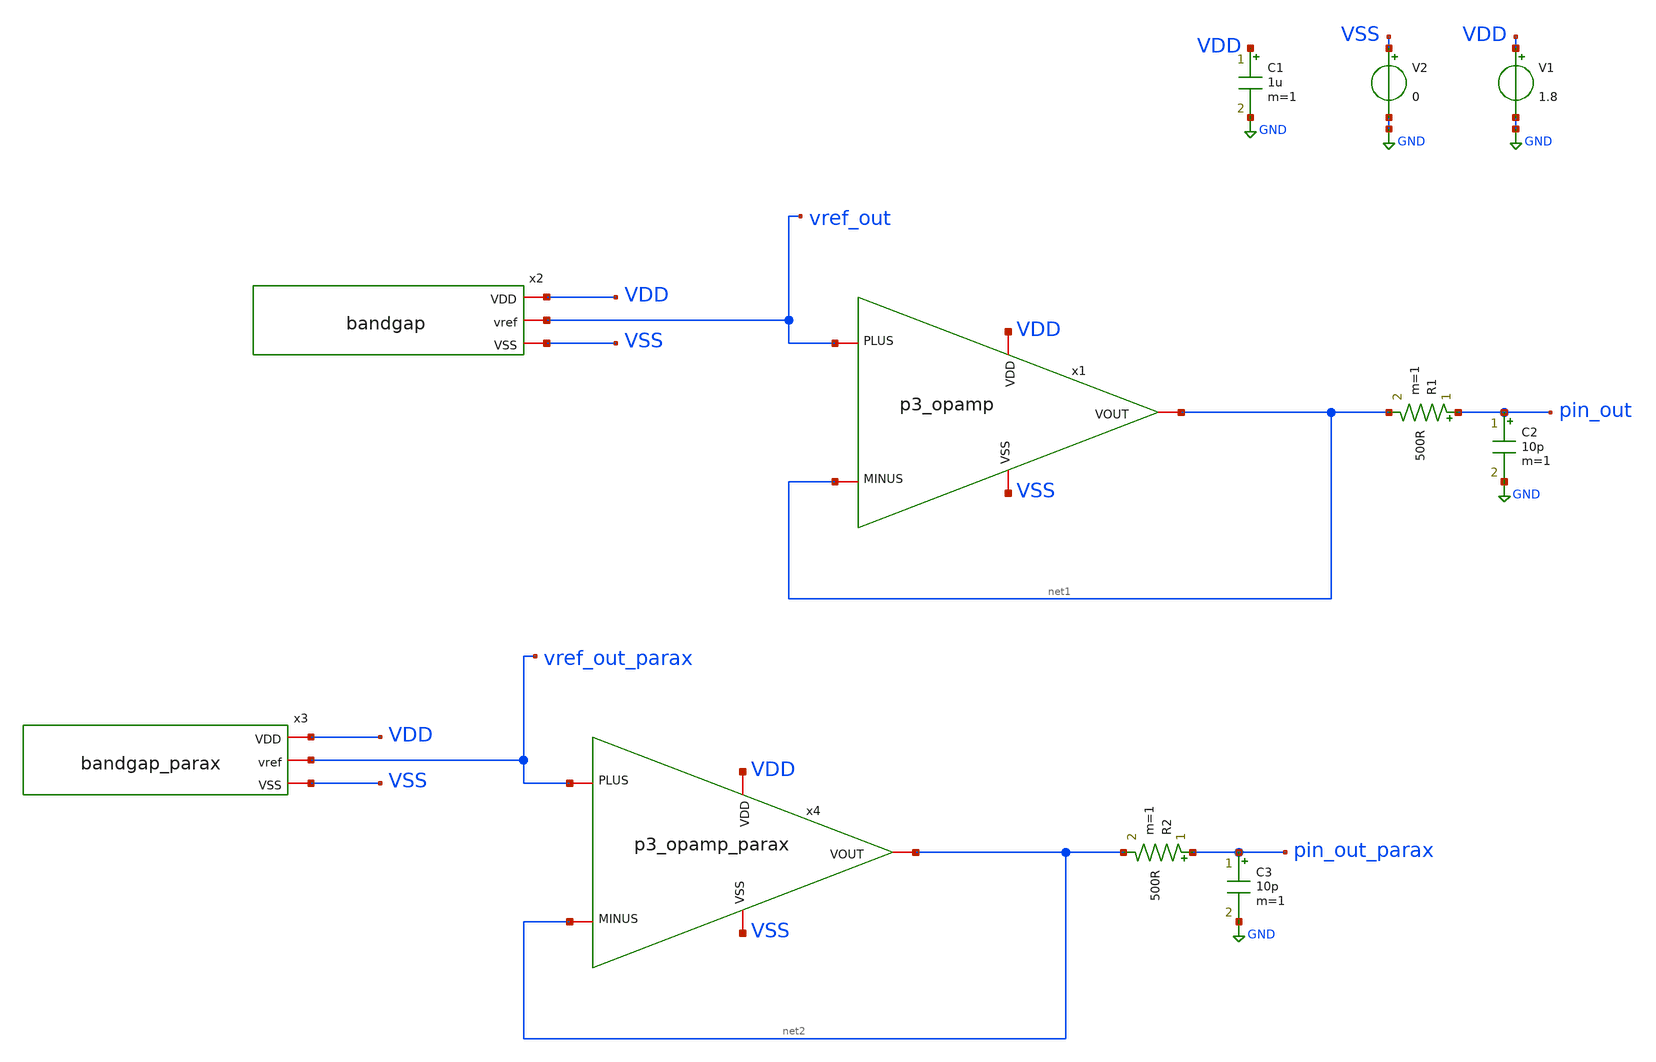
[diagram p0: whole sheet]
** sch_path: xschem/tb_bandgap.sch
**.subckt tb_bandgap
x2 VDD vref_out VSS bandgap
V1 VDD GND 1.8
V2 VSS GND 0
C1 VDD GND 1u m=1
x1 VDD net1 vref_out net1 VSS p3_opamp
R1 pin_out net1 500R m=1
C2 pin_out GND 10p m=1
x3 VDD vref_out_parax VSS bandgap_parax
x4 VDD net2 vref_out_parax net2 VSS p3_opamp_parax
R2 pin_out_parax net2 500R m=1
C3 pin_out_parax GND 10p m=1
**** begin user architecture code

** opencircuitdesign pdks install
.lib $::SKYWATER_MODELS/sky130.lib.spice tt






.control

 dc v1 1.3 2 0.01
 write tb_bandgap.raw
 set appendwrite

 reset
 dc temp 10 100 1
 write tb_bandgap.raw

.endc



**** end user architecture code
**.ends

* expanding   symbol:  bandgap.sym # of pins=3
** sym_path: xschem/bandgap.sym
** sch_path: xschem/bandgap.sch
.subckt bandgap VDD vref VSS
*.iopin VSS
*.iopin VDD
*.iopin vref
XM1 top_gate top_gate VDD VDD sky130_fd_pr__pfet_01v8 L=10 W=10 nf=1 ad='int((nf+1)/2) * W/nf * 0.29'
+ as='int((nf+2)/2) * W/nf * 0.29' pd='2*int((nf+1)/2) * (W/nf + 0.29)' ps='2*int((nf+2)/2) * (W/nf + 0.29)'
+ nrd='0.29 / W' nrs='0.29 / W' sa=0 sb=0 sd=0 mult=1 m=1
XM2 n_gate top_gate VDD VDD sky130_fd_pr__pfet_01v8 L=10 W=10 nf=1 ad='int((nf+1)/2) * W/nf * 0.29' as='int((nf+2)/2) * W/nf * 0.29'
+ pd='2*int((nf+1)/2) * (W/nf + 0.29)' ps='2*int((nf+2)/2) * (W/nf + 0.29)' nrd='0.29 / W' nrs='0.29 / W'
+ sa=0 sb=0 sd=0 mult=1 m=1
XM3 vref top_gate VDD VDD sky130_fd_pr__pfet_01v8 L=10 W=10 nf=1 ad='int((nf+1)/2) * W/nf * 0.29' as='int((nf+2)/2) * W/nf * 0.29'
+ pd='2*int((nf+1)/2) * (W/nf + 0.29)' ps='2*int((nf+2)/2) * (W/nf + 0.29)' nrd='0.29 / W' nrs='0.29 / W'
+ sa=0 sb=0 sd=0 mult=1 m=1
XR4 r4_m6 Va VSS sky130_fd_pr__res_high_po_0p69 L=204 mult=1 m=1
XR1 r1_m8 vref VSS sky130_fd_pr__res_high_po_0p69 L=204 mult=1 m=1
XM9 top_gate n_gate Va VSS sky130_fd_pr__nfet_01v8_lvt L=5 W=10 nf=1 ad='int((nf+1)/2) * W/nf * 0.29'
+ as='int((nf+2)/2) * W/nf * 0.29' pd='2*int((nf+1)/2) * (W/nf + 0.29)' ps='2*int((nf+2)/2) * (W/nf + 0.29)'
+ nrd='0.29 / W' nrs='0.29 / W' sa=0 sb=0 sd=0 mult=1 m=1
XM4 n_gate n_gate Vb VSS sky130_fd_pr__nfet_01v8_lvt L=5 W=10 nf=1 ad='int((nf+1)/2) * W/nf * 0.29' as='int((nf+2)/2) * W/nf * 0.29'
+ pd='2*int((nf+1)/2) * (W/nf + 0.29)' ps='2*int((nf+2)/2) * (W/nf + 0.29)' nrd='0.29 / W' nrs='0.29 / W'
+ sa=0 sb=0 sd=0 mult=1 m=1
XM5 VSS VSS r4_m6 VDD sky130_fd_pr__pfet_01v8_lvt L=5 W=10 nf=1 ad='int((nf+1)/2) * W/nf * 0.29' as='int((nf+2)/2) * W/nf * 0.29'
+ pd='2*int((nf+1)/2) * (W/nf + 0.29)' ps='2*int((nf+2)/2) * (W/nf + 0.29)' nrd='0.29 / W' nrs='0.29 / W'
+ sa=0 sb=0 sd=0 mult=1 m=1
XM6 VSS VSS r1_m8 VDD sky130_fd_pr__pfet_01v8_lvt L=5 W=10 nf=1 ad='int((nf+1)/2) * W/nf * 0.29' as='int((nf+2)/2) * W/nf * 0.29'
+ pd='2*int((nf+1)/2) * (W/nf + 0.29)' ps='2*int((nf+2)/2) * (W/nf + 0.29)' nrd='0.29 / W' nrs='0.29 / W'
+ sa=0 sb=0 sd=0 mult=1 m=1
XM7 VSS VSS Vb VDD sky130_fd_pr__pfet_01v8_lvt L=5 W=3 nf=1 ad='int((nf+1)/2) * W/nf * 0.29' as='int((nf+2)/2) * W/nf * 0.29'
+ pd='2*int((nf+1)/2) * (W/nf + 0.29)' ps='2*int((nf+2)/2) * (W/nf + 0.29)' nrd='0.29 / W' nrs='0.29 / W'
+ sa=0 sb=0 sd=0 mult=1 m=1
.ends


* expanding   symbol:  p3_opamp.sym # of pins=5
** sym_path: xschem/p3_opamp.sym
** sch_path: xschem/p3_opamp.sch
.subckt p3_opamp VDD MINUS PLUS VOUT VSS
*.iopin VDD
*.iopin VSS
*.iopin PLUS
*.iopin MINUS
*.iopin VOUT
XM3 VX VBIAS VSS VSS sky130_fd_pr__nfet_01v8 L=2 W=4 nf=4 ad='int((nf+1)/2) * W/nf * 0.29' as='int((nf+2)/2) * W/nf * 0.29'
+ pd='2*int((nf+1)/2) * (W/nf + 0.29)' ps='2*int((nf+2)/2) * (W/nf + 0.29)' nrd='0.29 / W' nrs='0.29 / W'
+ sa=0 sb=0 sd=0 mult=1 m=1
XM6 VBIAS VBIAS VSS VSS sky130_fd_pr__nfet_01v8 L=2 W=4 nf=4 ad='int((nf+1)/2) * W/nf * 0.29' as='int((nf+2)/2) * W/nf * 0.29'
+ pd='2*int((nf+1)/2) * (W/nf + 0.29)' ps='2*int((nf+2)/2) * (W/nf + 0.29)' nrd='0.29 / W' nrs='0.29 / W'
+ sa=0 sb=0 sd=0 mult=1 m=1
XM7 VOUT VBIAS VSS VSS sky130_fd_pr__nfet_01v8 L=2 W=7 nf=7 ad='int((nf+1)/2) * W/nf * 0.29' as='int((nf+2)/2) * W/nf * 0.29'
+ pd='2*int((nf+1)/2) * (W/nf + 0.29)' ps='2*int((nf+2)/2) * (W/nf + 0.29)' nrd='0.29 / W' nrs='0.29 / W'
+ sa=0 sb=0 sd=0 mult=1 m=1
XR1 VBIAS VDD VSS sky130_fd_pr__res_xhigh_po_0p35 L=2.8 mult=1 m=1
XM2 V2 MINUS VX VSS sky130_fd_pr__nfet_01v8_lvt L=0.5 W=2.5 nf=1 ad='int((nf+1)/2) * W/nf * 0.29' as='int((nf+2)/2) * W/nf * 0.29'
+ pd='2*int((nf+1)/2) * (W/nf + 0.29)' ps='2*int((nf+2)/2) * (W/nf + 0.29)' nrd='0.29 / W' nrs='0.29 / W'
+ sa=0 sb=0 sd=0 mult=1 m=1
XM1 V1 PLUS VX VSS sky130_fd_pr__nfet_01v8_lvt L=0.5 W=2.5 nf=1 ad='int((nf+1)/2) * W/nf * 0.29' as='int((nf+2)/2) * W/nf * 0.29'
+ pd='2*int((nf+1)/2) * (W/nf + 0.29)' ps='2*int((nf+2)/2) * (W/nf + 0.29)' nrd='0.29 / W' nrs='0.29 / W'
+ sa=0 sb=0 sd=0 mult=1 m=1
XM4 V2 V2 VDD VDD sky130_fd_pr__pfet_01v8_lvt L=2 W=6 nf=6 ad='int((nf+1)/2) * W/nf * 0.29' as='int((nf+2)/2) * W/nf * 0.29'
+ pd='2*int((nf+1)/2) * (W/nf + 0.29)' ps='2*int((nf+2)/2) * (W/nf + 0.29)' nrd='0.29 / W' nrs='0.29 / W'
+ sa=0 sb=0 sd=0 mult=1 m=1
XM5 V1 V2 VDD VDD sky130_fd_pr__pfet_01v8_lvt L=2 W=6 nf=6 ad='int((nf+1)/2) * W/nf * 0.29' as='int((nf+2)/2) * W/nf * 0.29'
+ pd='2*int((nf+1)/2) * (W/nf + 0.29)' ps='2*int((nf+2)/2) * (W/nf + 0.29)' nrd='0.29 / W' nrs='0.29 / W'
+ sa=0 sb=0 sd=0 mult=1 m=1
XM8 VOUT V1 VDD VDD sky130_fd_pr__pfet_01v8_lvt L=0.5 W=20 nf=20 ad='int((nf+1)/2) * W/nf * 0.29' as='int((nf+2)/2) * W/nf * 0.29'
+ pd='2*int((nf+1)/2) * (W/nf + 0.29)' ps='2*int((nf+2)/2) * (W/nf + 0.29)' nrd='0.29 / W' nrs='0.29 / W'
+ sa=0 sb=0 sd=0 mult=1 m=1
.ends


* expanding   symbol:  bandgap_parax.sym # of pins=3
** sym_path: xschem/bandgap.sym
.include [file normalize ../mag/bandgap.sim.spice]

* expanding   symbol:  p3_opamp_parax.sym # of pins=5
** sym_path: xschem/p3_opamp.sym
.include [file normalize ../mag/p3_opamp.sim.spice]
.GLOBAL GND
.end
